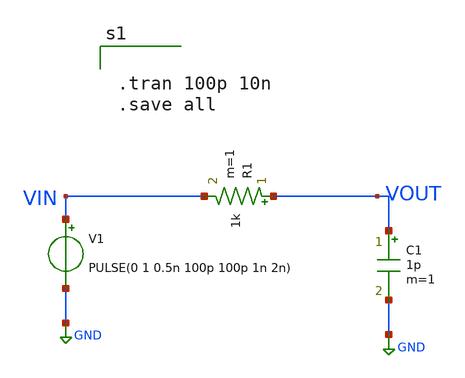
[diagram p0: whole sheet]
** sch_path: rc_ckt/rc_ckt.sch
**.subckt rc_ckt
R1 VOUT VIN 1k m=1
C1 VOUT GND 1p m=1
V1 VIN GND PULSE(0 1 0.5n 100p 100p 1n 2n)
**** begin user architecture code


.tran 100p 10n
.save all


**** end user architecture code
**.ends
.GLOBAL GND
.end
